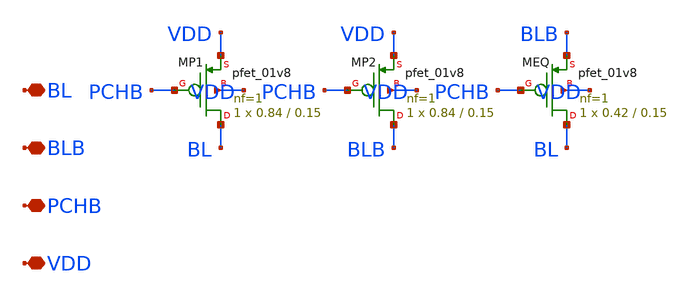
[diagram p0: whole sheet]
** sch_path: design/compiler/cells/sram_precharge.sch
**.subckt sram_precharge BL BLB PCHB VDD
*.iopin BL
*.iopin BLB
*.iopin PCHB
*.iopin VDD
XMP1 BL PCHB VDD VDD sky130_fd_pr__pfet_01v8 L=0.15 W=0.84 nf=1 ad=0.2436 as=0.2436 pd=2.26 ps=2.26
+ nrd=0.3452 nrs=0.3452 sa=0 sb=0 sd=0 mult=1 m=1
XMP2 BLB PCHB VDD VDD sky130_fd_pr__pfet_01v8 L=0.15 W=0.84 nf=1 ad=0.2436 as=0.2436 pd=2.26 ps=2.26
+ nrd=0.3452 nrs=0.3452 sa=0 sb=0 sd=0 mult=1 m=1
XMEQ BL PCHB BLB VDD sky130_fd_pr__pfet_01v8 L=0.15 W=0.42 nf=1 ad=0.1218 as=0.1218 pd=1.42 ps=1.42
+ nrd=0.6905 nrs=0.6905 sa=0 sb=0 sd=0 mult=1 m=1
**.ends
.end
